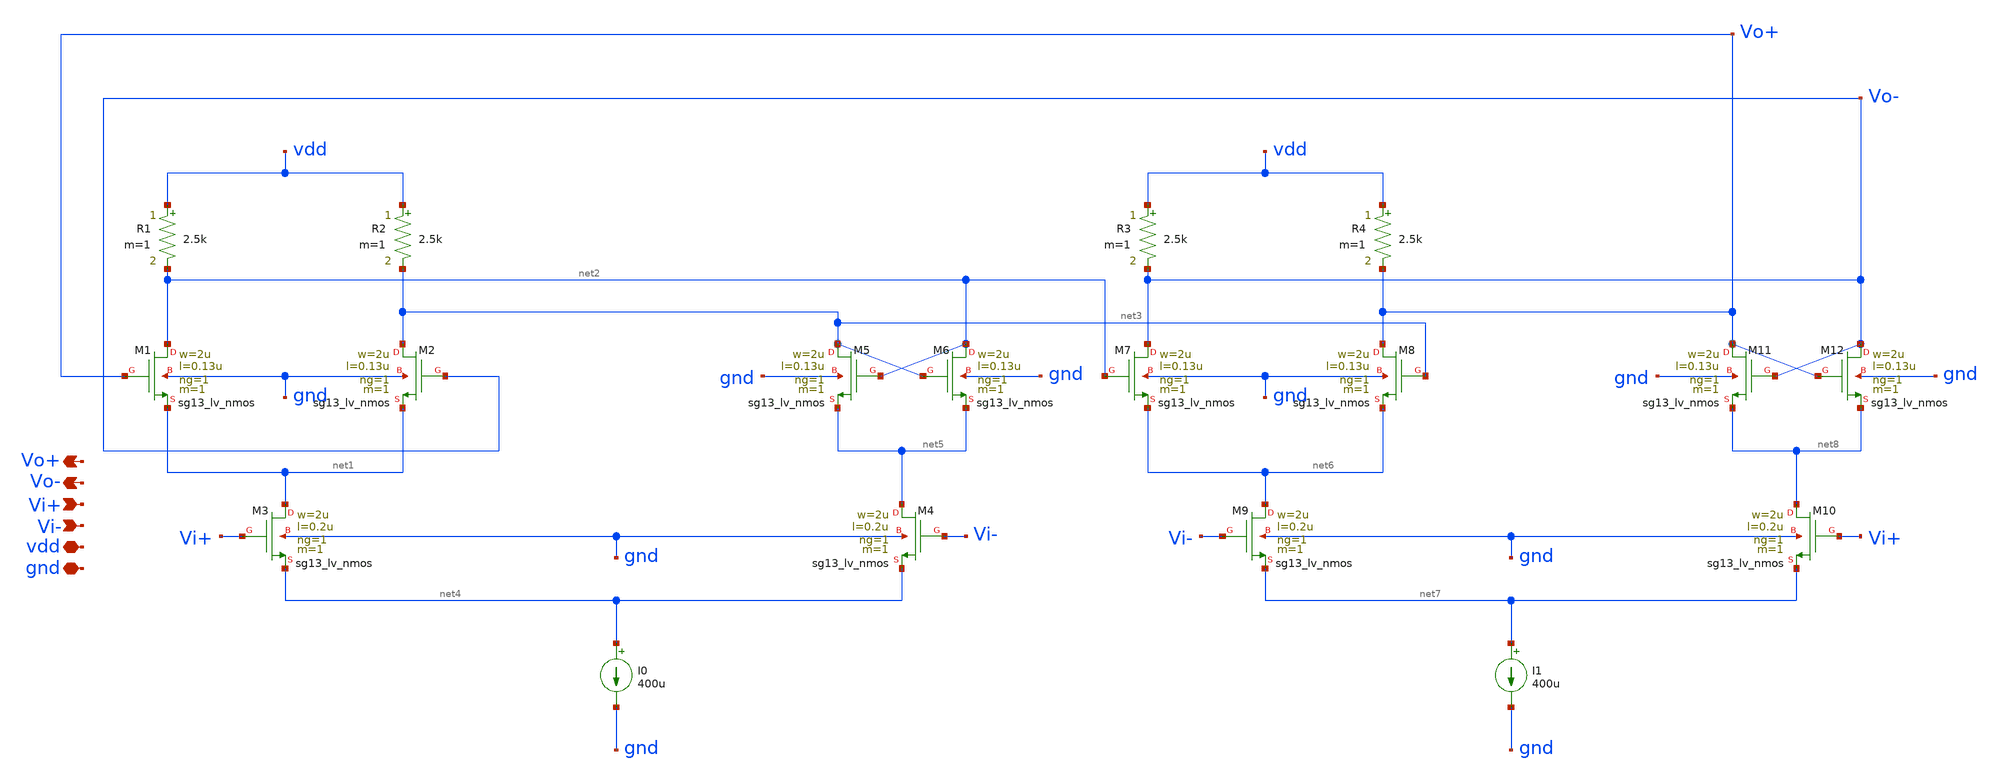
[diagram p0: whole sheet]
** sch_path: modules/module_4_type_2_PLL/CML_divider/xschem/CML_divider.sch
**.subckt CML_divider Vi+ Vi- Vo- vdd gnd Vo+
*.ipin Vi+
*.ipin Vi-
*.opin Vo-
*.iopin vdd
*.iopin gnd
*.opin Vo+
XM1 net2 Vo+ net1 gnd sg13_lv_nmos w=2u l=0.13u ng=1 m=1 mm_ok=1
XM2 net3 Vo- net1 gnd sg13_lv_nmos w=2u l=0.13u ng=1 m=1 mm_ok=1
R1 vdd net2 2.5k m=1
R2 vdd net3 2.5k m=1
XM3 net1 Vi+ net4 gnd sg13_lv_nmos w=2u l=0.2u ng=1 m=1 mm_ok=1
I0 net4 gnd 400u
XM4 net5 Vi- net4 gnd sg13_lv_nmos w=2u l=0.2u ng=1 m=1 mm_ok=1
XM5 net3 net2 net5 gnd sg13_lv_nmos w=2u l=0.13u ng=1 m=1 mm_ok=1
XM6 net2 net3 net5 gnd sg13_lv_nmos w=2u l=0.13u ng=1 m=1 mm_ok=1
XM7 Vo- net2 net6 gnd sg13_lv_nmos w=2u l=0.13u ng=1 m=1 mm_ok=1
XM8 Vo+ net3 net6 gnd sg13_lv_nmos w=2u l=0.13u ng=1 m=1 mm_ok=1
R3 vdd Vo- 2.5k m=1
R4 vdd Vo+ 2.5k m=1
XM9 net6 Vi- net7 gnd sg13_lv_nmos w=2u l=0.2u ng=1 m=1 mm_ok=1
I1 net7 gnd 400u
XM10 net8 Vi+ net7 gnd sg13_lv_nmos w=2u l=0.2u ng=1 m=1 mm_ok=1
XM11 Vo+ Vo- net8 gnd sg13_lv_nmos w=2u l=0.13u ng=1 m=1 mm_ok=1
XM12 Vo- Vo+ net8 gnd sg13_lv_nmos w=2u l=0.13u ng=1 m=1 mm_ok=1
**.ends
.end
